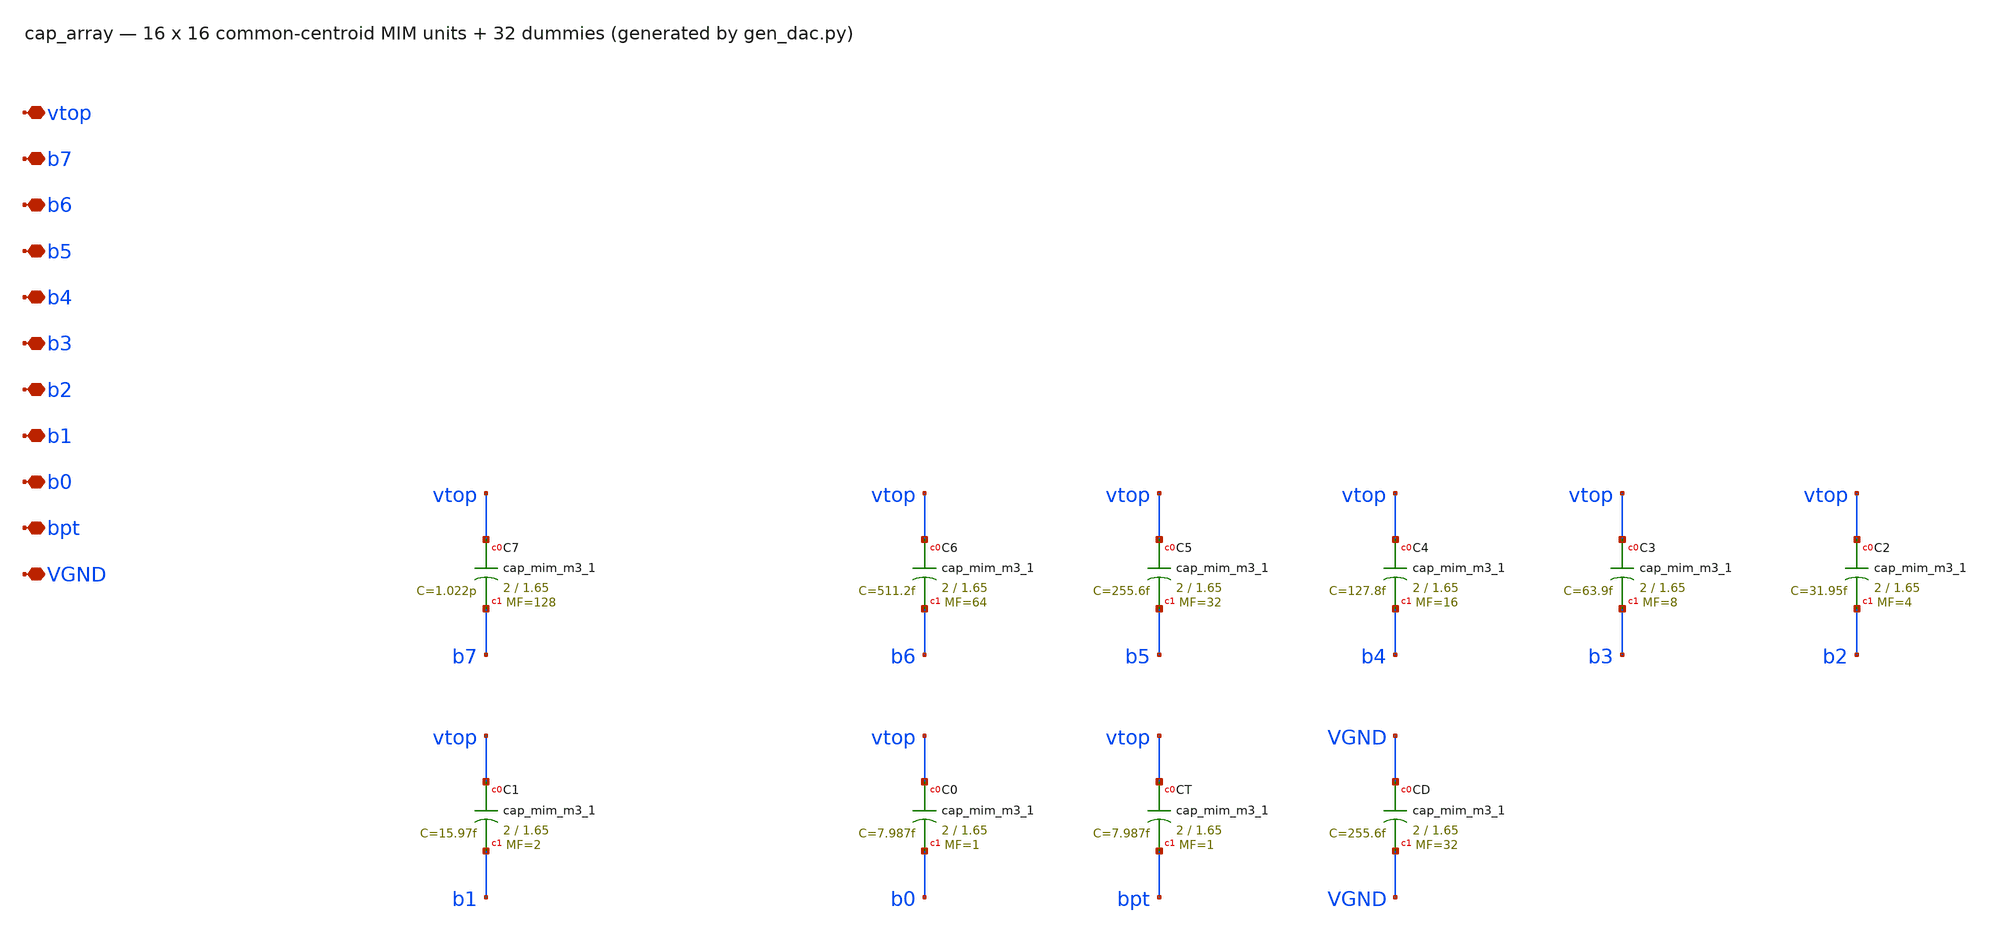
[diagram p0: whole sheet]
** sch_path: xschem/cap_array.sch
**.subckt cap_array vtop b7 b6 b5 b4 b3 b2 b1 b0 bpt VGND
*.iopin vtop
*.iopin b7
*.iopin b6
*.iopin b5
*.iopin b4
*.iopin b3
*.iopin b2
*.iopin b1
*.iopin b0
*.iopin bpt
*.iopin VGND
XC7 vtop b7 sky130_fd_pr__cap_mim_m3_1 W=2 L=1.65 MF=128 m=128
XC6 vtop b6 sky130_fd_pr__cap_mim_m3_1 W=2 L=1.65 MF=64 m=64
XC5 vtop b5 sky130_fd_pr__cap_mim_m3_1 W=2 L=1.65 MF=32 m=32
XC4 vtop b4 sky130_fd_pr__cap_mim_m3_1 W=2 L=1.65 MF=16 m=16
XC3 vtop b3 sky130_fd_pr__cap_mim_m3_1 W=2 L=1.65 MF=8 m=8
XC2 vtop b2 sky130_fd_pr__cap_mim_m3_1 W=2 L=1.65 MF=4 m=4
XC1 vtop b1 sky130_fd_pr__cap_mim_m3_1 W=2 L=1.65 MF=2 m=2
XC0 vtop b0 sky130_fd_pr__cap_mim_m3_1 W=2 L=1.65 MF=1 m=1
XCT vtop bpt sky130_fd_pr__cap_mim_m3_1 W=2 L=1.65 MF=1 m=1
XCD VGND VGND sky130_fd_pr__cap_mim_m3_1 W=2 L=1.65 MF=32 m=32
**.ends
.end
